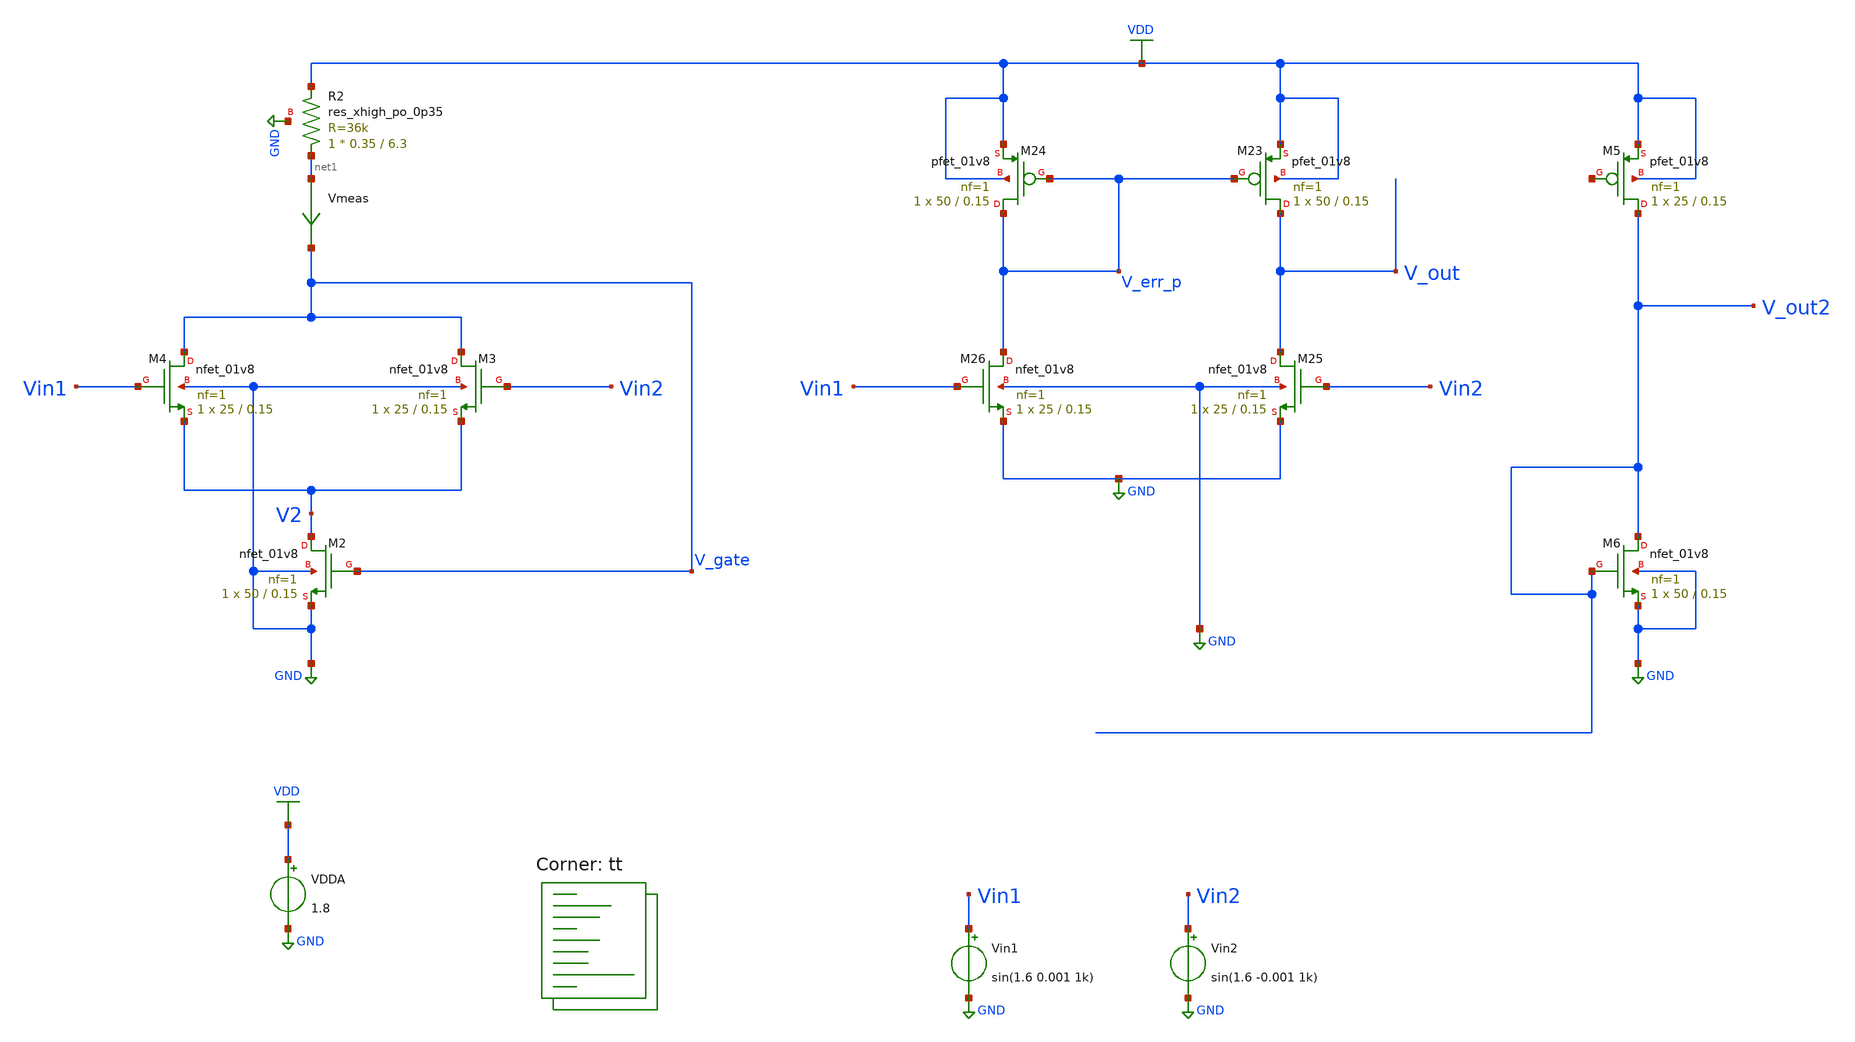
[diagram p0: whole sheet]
** sch_path: projects/bandgapref/xschem_ngspice/new_files/tb_opamp_bandgap.sch
**.subckt tb_opamp_bandgap
VDDA VDD GND 1.8
Vin1 Vin1 GND sin(1.6 0.001 1k)
Vin2 Vin2 GND sin(1.6 -0.001 1k)
XM23 V_out V_err_p VDD VDD sky130_fd_pr__pfet_01v8 L=0.15 W=50 nf=1 ad='int((nf+1)/2) * W/nf * 0.29'
+ as='int((nf+2)/2) * W/nf * 0.29' pd='2*int((nf+1)/2) * (W/nf + 0.29)' ps='2*int((nf+2)/2) * (W/nf + 0.29)'
+ nrd='0.29 / W' nrs='0.29 / W' sa=0 sb=0 sd=0 mult=1 m=1
XM24 V_err_p V_err_p VDD VDD sky130_fd_pr__pfet_01v8 L=0.15 W=50 nf=1 ad='int((nf+1)/2) * W/nf * 0.29'
+ as='int((nf+2)/2) * W/nf * 0.29' pd='2*int((nf+1)/2) * (W/nf + 0.29)' ps='2*int((nf+2)/2) * (W/nf + 0.29)'
+ nrd='0.29 / W' nrs='0.29 / W' sa=0 sb=0 sd=0 mult=1 m=1
XM25 V_out Vin2 GND GND sky130_fd_pr__nfet_01v8 L=0.15 W=25 nf=1 ad='int((nf+1)/2) * W/nf * 0.29' as='int((nf+2)/2) * W/nf * 0.29'
+ pd='2*int((nf+1)/2) * (W/nf + 0.29)' ps='2*int((nf+2)/2) * (W/nf + 0.29)' nrd='0.29 / W' nrs='0.29 / W'
+ sa=0 sb=0 sd=0 mult=1 m=1
XM26 V_err_p Vin1 GND GND sky130_fd_pr__nfet_01v8 L=0.15 W=25 nf=1 ad='int((nf+1)/2) * W/nf * 0.29' as='int((nf+2)/2) * W/nf * 0.29'
+ pd='2*int((nf+1)/2) * (W/nf + 0.29)' ps='2*int((nf+2)/2) * (W/nf + 0.29)' nrd='0.29 / W' nrs='0.29 / W'
+ sa=0 sb=0 sd=0 mult=1 m=1
XM2 V2 V_gate GND GND sky130_fd_pr__nfet_01v8 L=0.15 W=50 nf=1 ad='int((nf+1)/2) * W/nf * 0.29' as='int((nf+2)/2) * W/nf * 0.29'
+ pd='2*int((nf+1)/2) * (W/nf + 0.29)' ps='2*int((nf+2)/2) * (W/nf + 0.29)' nrd='0.29 / W' nrs='0.29 / W'
+ sa=0 sb=0 sd=0 mult=1 m=1
Vmeas net1 V_gate 0
.save i(vmeas)
XR2 net1 VDD GND sky130_fd_pr__res_xhigh_po_0p35 L=6.3 mult=1 m=1
XM3 V_gate Vin2 V2 GND sky130_fd_pr__nfet_01v8 L=0.15 W=25 nf=1 ad='int((nf+1)/2) * W/nf * 0.29' as='int((nf+2)/2) * W/nf * 0.29'
+ pd='2*int((nf+1)/2) * (W/nf + 0.29)' ps='2*int((nf+2)/2) * (W/nf + 0.29)' nrd='0.29 / W' nrs='0.29 / W'
+ sa=0 sb=0 sd=0 mult=1 m=1
XM4 V_gate Vin1 V2 GND sky130_fd_pr__nfet_01v8 L=0.15 W=25 nf=1 ad='int((nf+1)/2) * W/nf * 0.29' as='int((nf+2)/2) * W/nf * 0.29'
+ pd='2*int((nf+1)/2) * (W/nf + 0.29)' ps='2*int((nf+2)/2) * (W/nf + 0.29)' nrd='0.29 / W' nrs='0.29 / W'
+ sa=0 sb=0 sd=0 mult=1 m=1
XM5 V_out2 net2 VDD VDD sky130_fd_pr__pfet_01v8 L=0.15 W=25 nf=1 ad='int((nf+1)/2) * W/nf * 0.29' as='int((nf+2)/2) * W/nf * 0.29'
+ pd='2*int((nf+1)/2) * (W/nf + 0.29)' ps='2*int((nf+2)/2) * (W/nf + 0.29)' nrd='0.29 / W' nrs='0.29 / W'
+ sa=0 sb=0 sd=0 mult=1 m=1
XM6 V_out2 V_out2 GND GND sky130_fd_pr__nfet_01v8 L=0.15 W=50 nf=1 ad='int((nf+1)/2) * W/nf * 0.29' as='int((nf+2)/2) * W/nf * 0.29'
+ pd='2*int((nf+1)/2) * (W/nf + 0.29)' ps='2*int((nf+2)/2) * (W/nf + 0.29)' nrd='0.29 / W' nrs='0.29 / W'
+ sa=0 sb=0 sd=0 mult=1 m=1
**** begin user architecture code



.option wnflag=1
.option savecurrents

* .param VDDGAUSS = agauss(1.8, 0.05, 1)
* .param VDD = VDDGAUSS
* .param VDD = 1.8

* .param TEMPGAUSS = agauss(40, 30, 1)
* .param temp = TEMPGAUSS
.option temp = 26

.save @m.x1.xm1.msky130_fd_pr__nfet_01v8[gm] @m.x1.xm2.msky130_fd_pr__nfet_01v8[gm] @m.x1.xm3.msky130_fd_pr__nfet_01v8[gm] @m.x1.xm4.msky130_fd_pr__pfet_01v8[gm] @m.x1.xm5.msky130_fd_pr__pfet_01v8[gm] @m.x1.xm6.msky130_fd_pr__nfet_01v8[gm] @m.x1.xm7.msky130_fd_pr__pfet_01v8[gm]

.control

  save all
   tran 1u 10m
   * ac dec 20 1 1T

  write tb_opamp_bandgap.raw
  set appendwrite

.endc



.lib $::SKYWATER_MODELS/sky130.lib.spice tt
**** end user architecture code
**.ends
.GLOBAL GND
.GLOBAL VDD
.end
